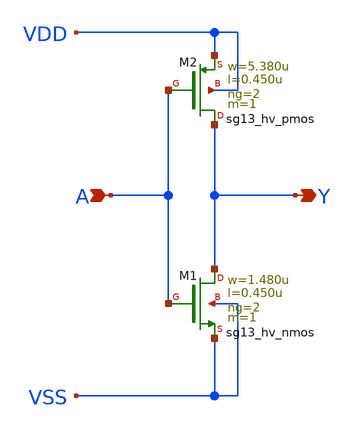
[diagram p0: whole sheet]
** sch_path: ihp-sg13g2/libs.ref/sg13g2_stdcell_hv/sch/xschem/sg13g2_hv_inv_2.sch
* Copyright 2023 IHP PDK Authors
* Licensed under the Apache License, Version 2.0 (the "License");
* you may not use this file except in compliance with the License.
* You may obtain a copy of the License at
* https://www.apache.org/licenses/LICENSE-2.0
* Unless required by applicable law or agreed to in writing, software
* distributed under the License is distributed on an "AS IS" BASIS,
* WITHOUT WARRANTIES OR CONDITIONS OF ANY KIND, either express or implied.
* See the License for the specific language governing permissions and
* limitations under the License.
**.subckt sg13g2_hv_inv_2 Y A
*.opin Y
*.ipin A
XM1 Y A VSS VSS sg13_hv_nmos w=1.480u l=0.450u ng=2 m=1 mm_ok=1
XM2 Y A VDD VDD sg13_hv_pmos w=5.380u l=0.450u ng=2 m=1 mm_ok=1
**.ends
.end
